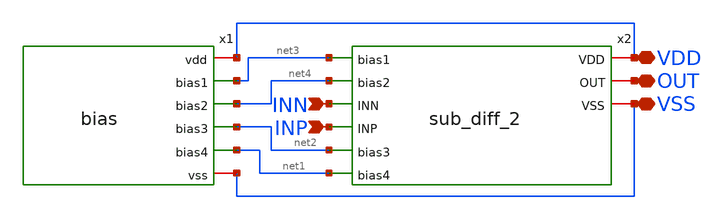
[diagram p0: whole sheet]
** sch_path: FINAL/XSCHEM/OPAM/OPAMt.sch
**.subckt OPAMt INN INP VDD VSS OUT
*.ipin INN
*.ipin INP
*.iopin VDD
*.iopin VSS
*.iopin OUT
x1 VDD net3 net4 net2 net1 VSS bias
x2 VDD net3 net4 OUT INN INP net2 net1 VSS sub_diff_2
**.ends
.end
